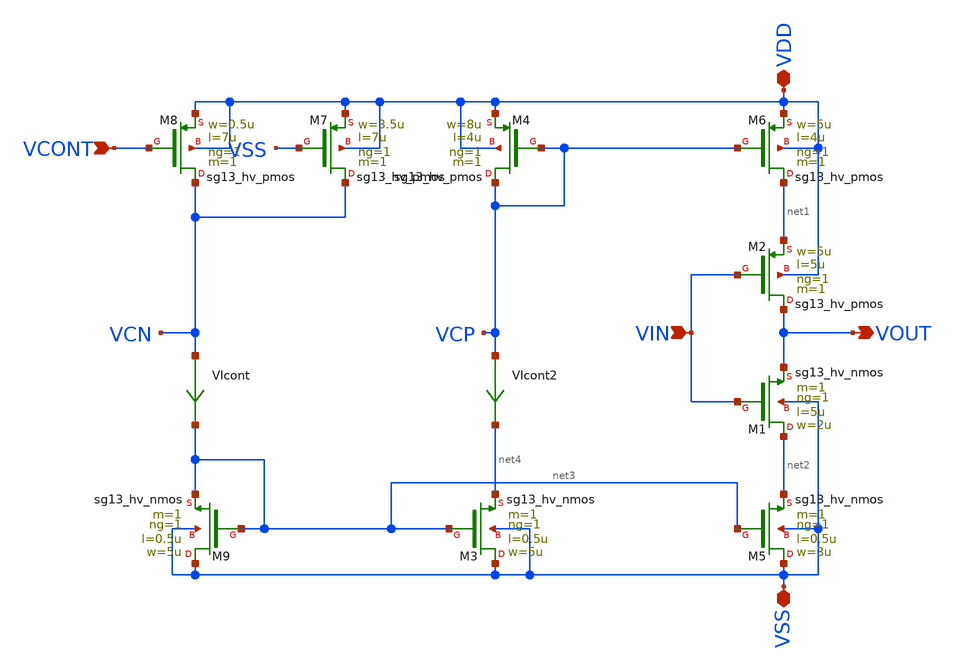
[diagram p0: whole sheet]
** sch_path: xschem/VCO/stage_vto1p1.sch
**.subckt stage_vto1p1 VIN VOUT VDD VSS VCONT
*.ipin VIN
*.opin VOUT
*.iopin VDD
*.iopin VSS
*.ipin VCONT
XM9 VSS net3 net3 VSS sg13_hv_nmos w=5u l=0.5u ng=1 m=1 mm_ok=1
XM3 VSS net3 net4 VSS sg13_hv_nmos w=5u l=0.5u ng=1 m=1 mm_ok=1
XM5 VSS net3 net2 VSS sg13_hv_nmos w=3u l=0.5u ng=1 m=1 mm_ok=1
XM8 VCN VCONT VDD VDD sg13_hv_pmos w=0.5u l=7u ng=1 m=1 mm_ok=1
XM4 VCP VCP VDD VDD sg13_hv_pmos w=8u l=4u ng=1 m=1 mm_ok=1
XM6 net1 VCP VDD VDD sg13_hv_pmos w=5u l=4u ng=1 m=1 mm_ok=1
XM2 VOUT VIN net1 VDD sg13_hv_pmos w=5u l=5u ng=1 m=1 mm_ok=1
XM1 net2 VIN VOUT VSS sg13_hv_nmos w=2u l=5u ng=1 m=1 mm_ok=1
XM7 VCN VSS VDD VDD sg13_hv_pmos w=3.5u l=7u ng=1 m=1 mm_ok=1
VIcont VCN net3 0
.save i(vicont)
VIcont2 VCP net4 0
.save i(vicont2)
**.ends
.end
